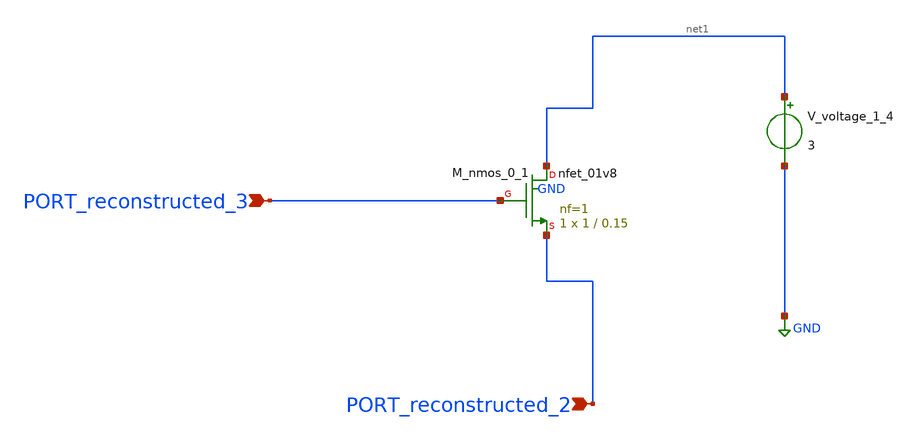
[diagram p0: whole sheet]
** sch_path: schematics/AMSNet/18.sch
**.subckt 18 PORT_reconstructed_3 PORT_reconstructed_2
*.ipin PORT_reconstructed_3
*.ipin PORT_reconstructed_2
XM_nmos_0_1 net1 PORT_reconstructed_3 PORT_reconstructed_2 GND sky130_fd_pr__nfet_01v8 L=0.15 W=1 nf=1
+ ad='int((1 + 1)/2) * 1 / 1 * 0.29' as='int((1 + 2)/2) * 1 / 1 * 0.29' pd='2*int((1 + 1)/2) * (1 / 1 + 0.29)'
+ ps='2*int((1 + 2)/2) * (1 / 1 + 0.29)' nrd='0.29 / 1 ' nrs='0.29 / 1 ' sa=0 sb=0 sd=0 mult=1 m=1
V_voltage_1_4 net1 GND 3
**.ends
.GLOBAL GND
.end
